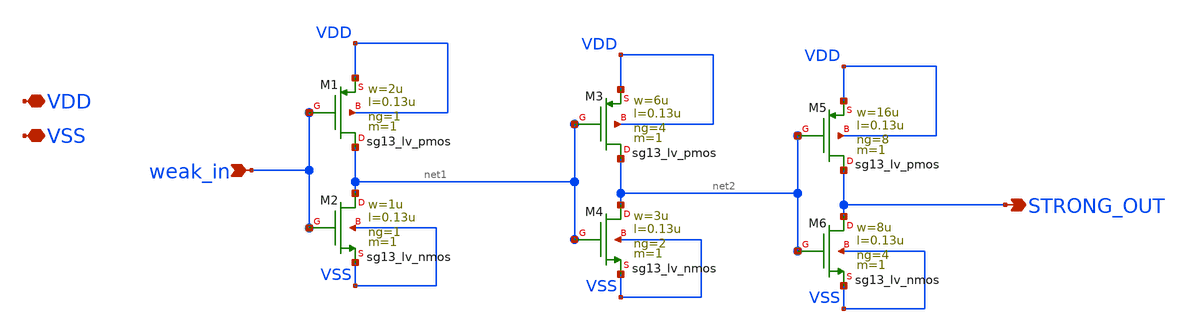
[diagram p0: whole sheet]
** sch_path: xschem/inverter_chain.sch
**.subckt inverter_chain VDD VSS weak_in STRONG_OUT
*.iopin VDD
*.iopin VSS
*.ipin weak_in
*.opin STRONG_OUT
XM1 net1 weak_in VDD VDD sg13_lv_pmos w=2u l=0.13u ng=1 m=1 mm_ok=1
XM2 net1 weak_in VSS VSS sg13_lv_nmos w=1u l=0.13u ng=1 m=1 mm_ok=1
XM3 net2 net1 VDD VDD sg13_lv_pmos w=6u l=0.13u ng=4 m=1 mm_ok=1
XM4 net2 net1 VSS VSS sg13_lv_nmos w=3u l=0.13u ng=2 m=1 mm_ok=1
XM5 STRONG_OUT net2 VDD VDD sg13_lv_pmos w=16u l=0.13u ng=8 m=1 mm_ok=1
XM6 STRONG_OUT net2 VSS VSS sg13_lv_nmos w=8u l=0.13u ng=4 m=1 mm_ok=1
**.ends
.end
